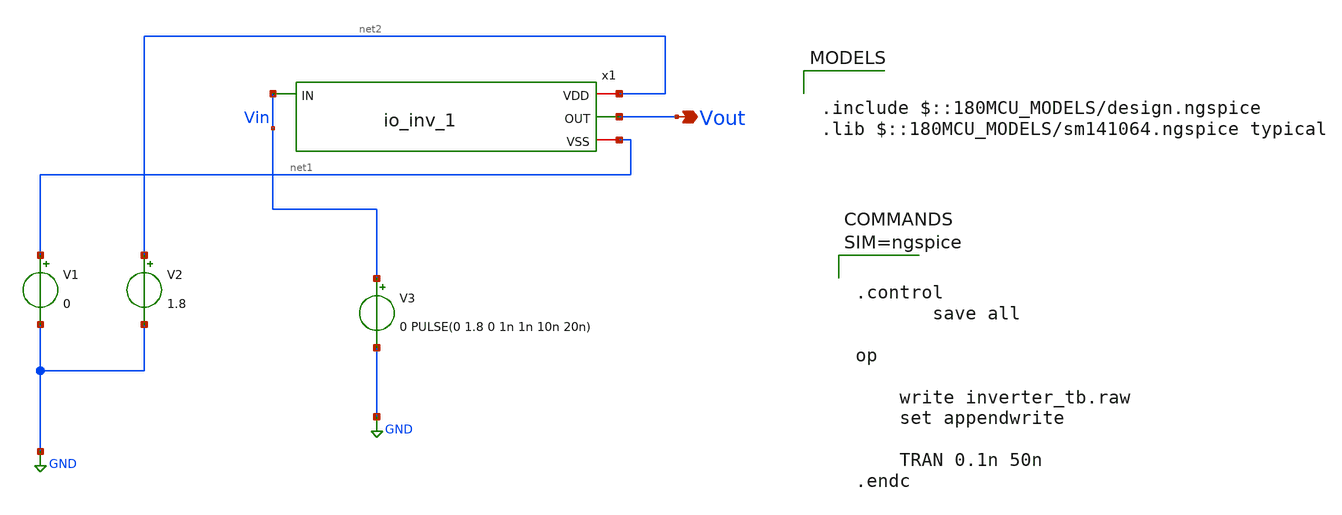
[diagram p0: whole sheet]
** sch_path: xschem/io_inv_1_tb.sch
* Copyright 2023 David Mitchell Bailey
* Licensed under the Apache License, Version 2.0 (the "License");
* you may not use this file except in compliance with the License.
* You may obtain a copy of the License at
* https://www.apache.org/licenses/LICENSE-2.0
* Unless required by applicable law or agreed to in writing, software
* distributed under the License is distributed on an "AS IS" BASIS,
* WITHOUT WARRANTIES OR CONDITIONS OF ANY KIND, either express or implied.
* See the License for the specific language governing permissions and
* limitations under the License.
**.subckt io_inv_1_tb Vout
*.opin Vout
x1 net2 Vout Vin net1 io_inv_1
V1 net1 GND 0
V2 net2 GND 1.8
V3 Vin GND 0 PULSE(0 1.8 0 1n 1n 10n 20n)
**** begin user architecture code

.include $::180MCU_MODELS/design.ngspice
.lib $::180MCU_MODELS/sm141064.ngspice typical




.control
	   save all

op

    write inverter_tb.raw
    set appendwrite

	TRAN 0.1n 50n
.endc




**** end user architecture code
**.ends

* expanding   symbol:  io_inv_1.sym # of pins=4
** sym_path: xschem/io_inv_1.sym
** sch_path: xschem/io_inv_1.sch
.subckt io_inv_1 VDD OUT IN VSS
*.opin OUT
*.ipin IN
*.iopin VDD
*.iopin VSS
XM2 OUT IN VSS VSS nfet_03v3 L=0.28u W=0.6u nf=1 ad='int((nf+1)/2) * W/nf * 0.18u' as='int((nf+2)/2) * W/nf * 0.18u'
+ pd='2*int((nf+1)/2) * (W/nf + 0.18u)' ps='2*int((nf+2)/2) * (W/nf + 0.18u)' nrd='0.18u / W' nrs='0.18u / W'
+ sa=0 sb=0 sd=0 m=1
XM4 OUT IN VDD VDD pfet_03v3 L=0.28u W=1.2u nf=1 ad='int((nf+1)/2) * W/nf * 0.18u' as='int((nf+2)/2) * W/nf * 0.18u'
+ pd='2*int((nf+1)/2) * (W/nf + 0.18u)' ps='2*int((nf+2)/2) * (W/nf + 0.18u)' nrd='0.18u / W' nrs='0.18u / W'
+ sa=0 sb=0 sd=0 m=1
.ends

.GLOBAL GND
.end
